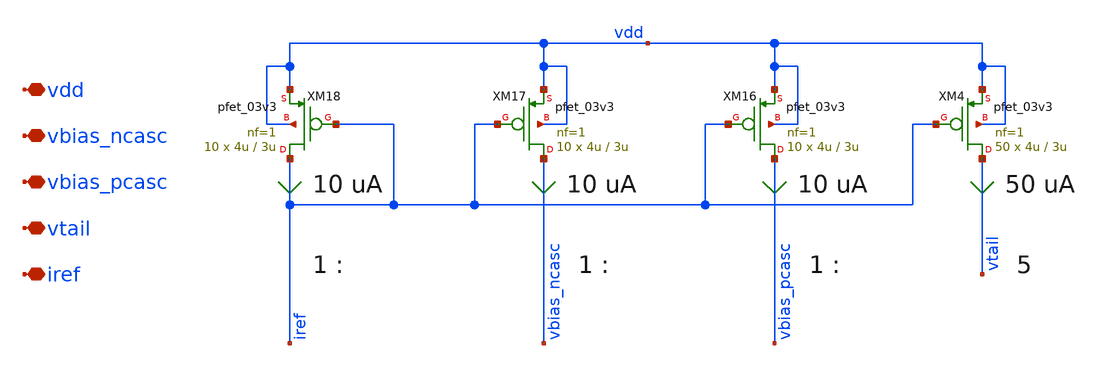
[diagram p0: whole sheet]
** sch_path: xschem/ccia_rrl_ota/b9_ccia_rrl_ota_pmos_bias.sch
**.subckt b9_ccia_rrl_ota_pmos_bias vdd vbias_ncasc vbias_pcasc vtail iref
*.iopin vdd
*.iopin vbias_ncasc
*.iopin vbias_pcasc
*.iopin vtail
*.iopin iref
XM4 vtail iref vdd vdd pfet_03v3 L=3u W=4u nf=1 ad='int((nf+1)/2) * W/nf * 0.18u' as='int((nf+2)/2) * W/nf * 0.18u'
+ pd='2*int((nf+1)/2) * (W/nf + 0.18u)' ps='2*int((nf+2)/2) * (W/nf + 0.18u)' nrd='0.18u / W' nrs='0.18u / W'
+ sa=0 sb=0 sd=0 m=50
XM16 vbias_pcasc iref vdd vdd pfet_03v3 L=3u W=4u nf=1 ad='int((nf+1)/2) * W/nf * 0.18u' as='int((nf+2)/2) * W/nf * 0.18u'
+ pd='2*int((nf+1)/2) * (W/nf + 0.18u)' ps='2*int((nf+2)/2) * (W/nf + 0.18u)' nrd='0.18u / W' nrs='0.18u / W'
+ sa=0 sb=0 sd=0 m=10
XM17 vbias_ncasc iref vdd vdd pfet_03v3 L=3u W=4u nf=1 ad='int((nf+1)/2) * W/nf * 0.18u' as='int((nf+2)/2) * W/nf * 0.18u'
+ pd='2*int((nf+1)/2) * (W/nf + 0.18u)' ps='2*int((nf+2)/2) * (W/nf + 0.18u)' nrd='0.18u / W' nrs='0.18u / W'
+ sa=0 sb=0 sd=0 m=10
XM18 iref iref vdd vdd pfet_03v3 L=3u W=4u nf=1 ad='int((nf+1)/2) * W/nf * 0.18u' as='int((nf+2)/2) * W/nf * 0.18u'
+ pd='2*int((nf+1)/2) * (W/nf + 0.18u)' ps='2*int((nf+2)/2) * (W/nf + 0.18u)' nrd='0.18u / W' nrs='0.18u / W'
+ sa=0 sb=0 sd=0 m=10
**.ends
.end
